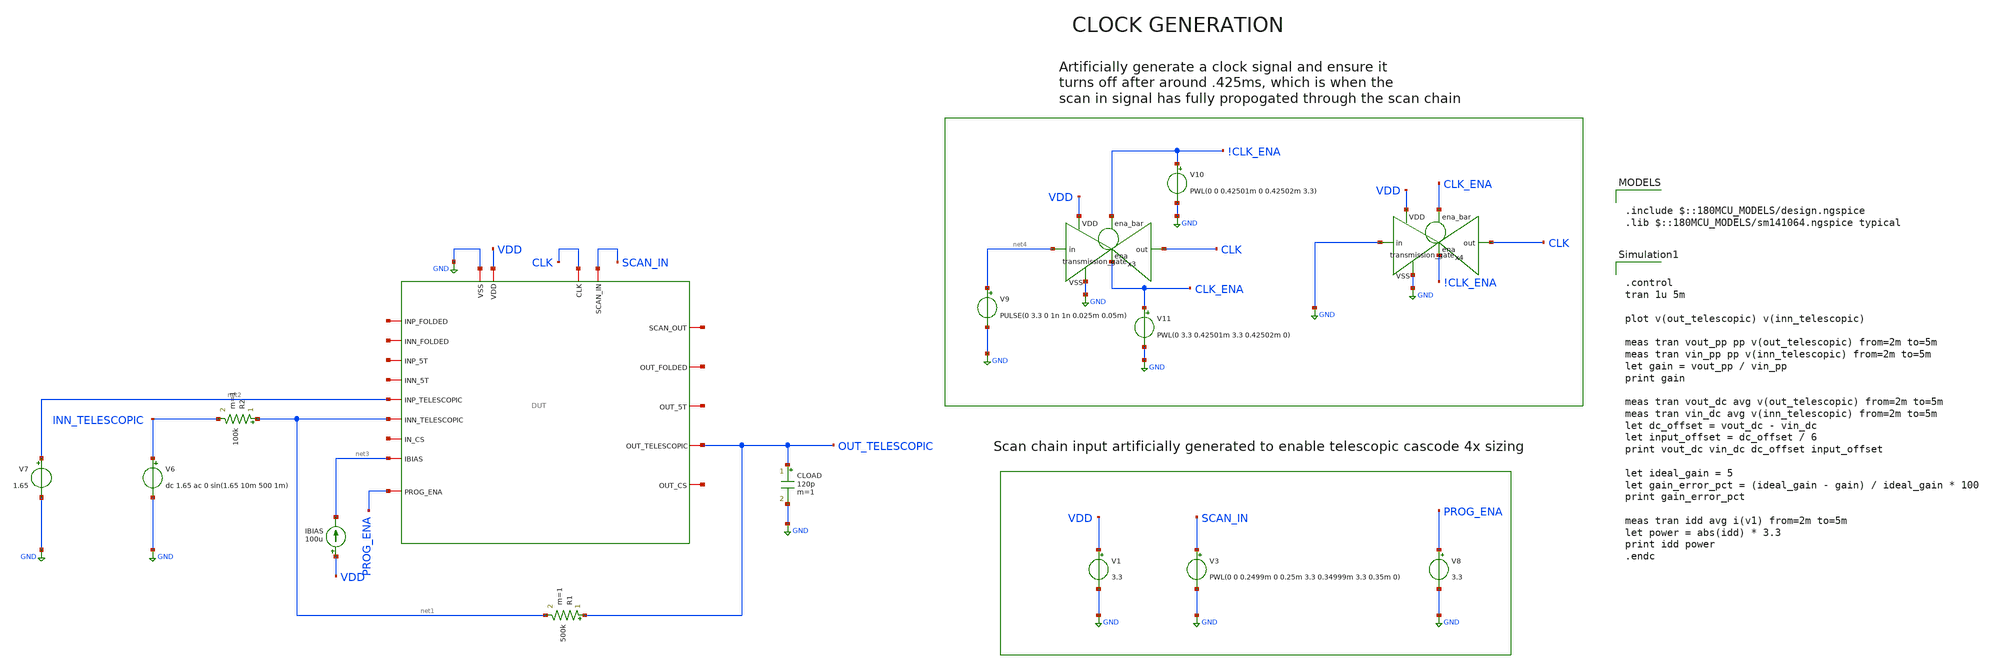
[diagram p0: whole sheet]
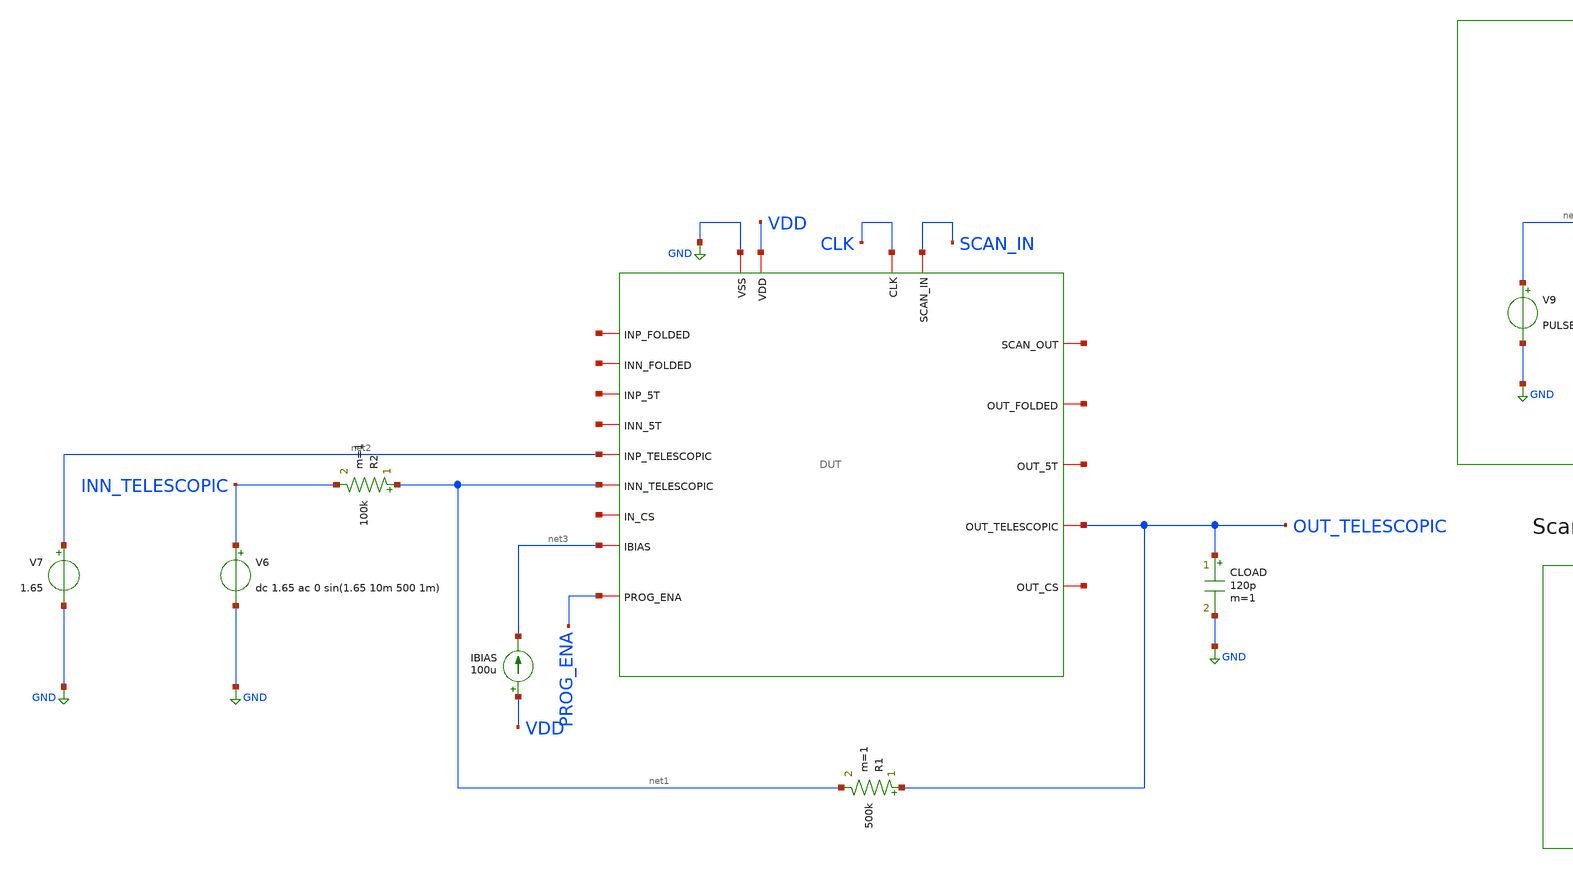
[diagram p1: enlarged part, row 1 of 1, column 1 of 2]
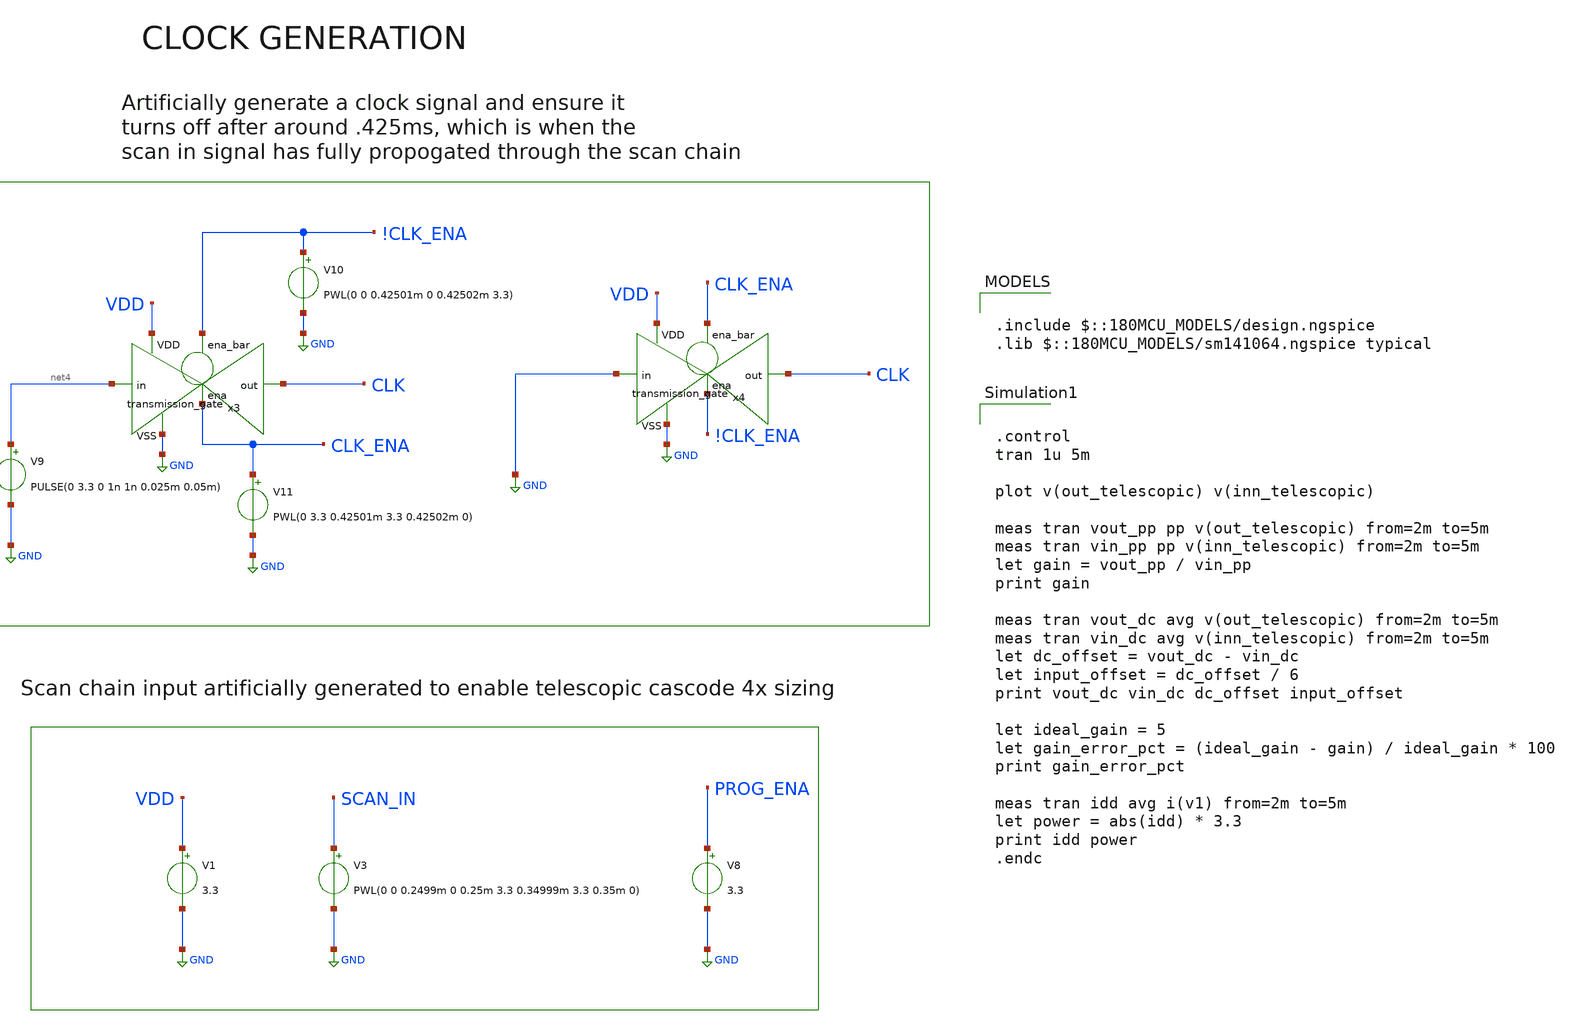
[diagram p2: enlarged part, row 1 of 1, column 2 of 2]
** sch_path: designs/libs/verification/ota_telescopic/4x/5x_inverting.sch
**.subckt 5x_inverting
x1 CLK net5 SCAN_IN GND VDD net6 net7 net8 net3 net9 net10 net11 net2 OUT_TELESCOPIC net12 net13
+ net1 PROG_ENA DUT
CLOAD OUT_TELESCOPIC GND 120p m=1
R1 OUT_TELESCOPIC net1 500k m=1
R2 net1 INN_TELESCOPIC 100k m=1
V6 INN_TELESCOPIC GND dc 1.65 ac 0 sin(1.65 10m 500 1m)
V7 net2 GND 1.65
IBIAS VDD net3 100u
V3 SCAN_IN GND PWL(0 0 0.2499m 0 0.25m 3.3 0.34999m 3.3 0.35m 0)
V1 VDD GND 3.3
V8 PROG_ENA GND 3.3
V9 net4 GND PULSE(0 3.3 0 1n 1n 0.025m 0.05m)
x3 !CLK_ENA VDD CLK net4 GND CLK_ENA transmission_gate
V10 !CLK_ENA GND PWL(0 0 0.42501m 0 0.42502m 3.3)
V11 CLK_ENA GND PWL(0 3.3 0.42501m 3.3 0.42502m 0)
x4 CLK_ENA VDD CLK GND GND !CLK_ENA transmission_gate
**** begin user architecture code

.include $::180MCU_MODELS/design.ngspice
.lib $::180MCU_MODELS/sm141064.ngspice typical



.control
tran 1u 5m

plot v(out_telescopic) v(inn_telescopic)

meas tran vout_pp pp v(out_telescopic) from=2m to=5m
meas tran vin_pp pp v(inn_telescopic) from=2m to=5m
let gain = vout_pp / vin_pp
print gain

meas tran vout_dc avg v(out_telescopic) from=2m to=5m
meas tran vin_dc avg v(inn_telescopic) from=2m to=5m
let dc_offset = vout_dc - vin_dc
let input_offset = dc_offset / 6
print vout_dc vin_dc dc_offset input_offset

let ideal_gain = 5
let gain_error_pct = (ideal_gain - gain) / ideal_gain * 100
print gain_error_pct

meas tran idd avg i(v1) from=2m to=5m
let power = abs(idd) * 3.3
print idd power
.endc


**** end user architecture code
**.ends
.GLOBAL GND
.end
